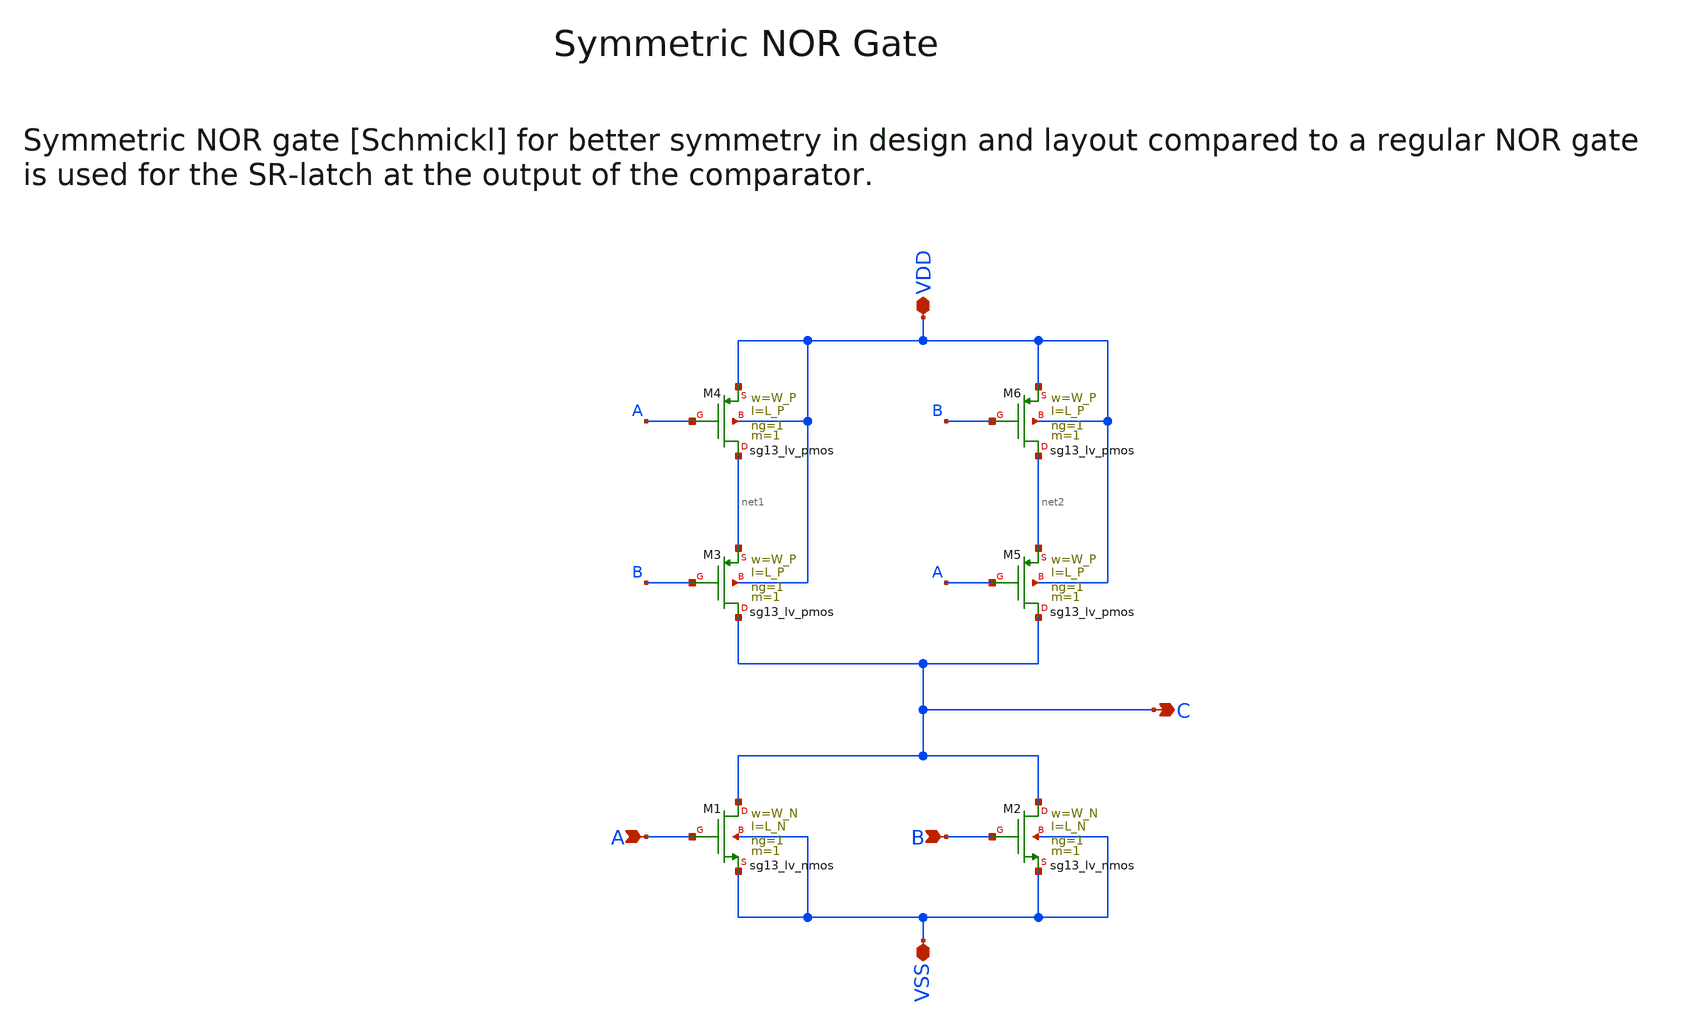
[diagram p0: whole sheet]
** sch_path: SG13G2_ATBS-ADC-main/xschem/comparator/NOR_gate/NOR_gate.sch
**.subckt NOR_gate VDD C VSS A B
*.iopin VDD
*.opin C
*.iopin VSS
*.ipin A
*.ipin B
XM1 C A VSS VSS sg13_lv_nmos w=W_N l=L_N ng=1 m=1 mm_ok=1
XM2 C B VSS VSS sg13_lv_nmos w=W_N l=L_N ng=1 m=1 mm_ok=1
XM3 C B net1 VDD sg13_lv_pmos w=W_P l=L_P ng=1 m=1 mm_ok=1
XM4 net1 A VDD VDD sg13_lv_pmos w=W_P l=L_P ng=1 m=1 mm_ok=1
XM5 C A net2 VDD sg13_lv_pmos w=W_P l=L_P ng=1 m=1 mm_ok=1
XM6 net2 B VDD VDD sg13_lv_pmos w=W_P l=L_P ng=1 m=1 mm_ok=1
**.ends
.end
